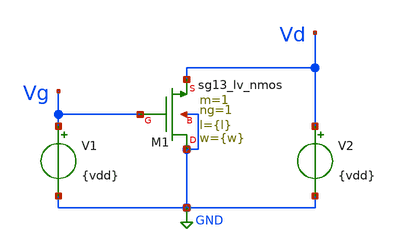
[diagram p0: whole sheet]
** sch_path: Parametros_Psp/zeda_test.sch
**.subckt zeda_test
V1 Vg GND {vdd}
V2 Vd GND {vdd}
XM1 GND Vg Vd GND sg13_lv_nmos w={w} l={l} ng=1 m=1 mm_ok=1
**** begin user architecture code


* Circuit Parameters
.param vdd = 1.2
.param w = 5.0u
.param l = 0.18u
* Include Models
.lib /opt/pdks/ihp-sg13g2/libs.tech/ngspice/models/cornerMOSlv.lib mos_tt
.lib /opt/pdks/ihp-sg13g2/libs.tech/ngspice/models/cornerMOShv.lib mos_tt
* OP Parameters & Singals to save
.save all
.save @n.xm1.nsg13_lv_nmos[ide]
*Simulations
.op
.control
run
set filetype = ascii
write dcsweep_v2.raw
.endc
.end


**** end user architecture code
**.ends
.GLOBAL GND
.end
